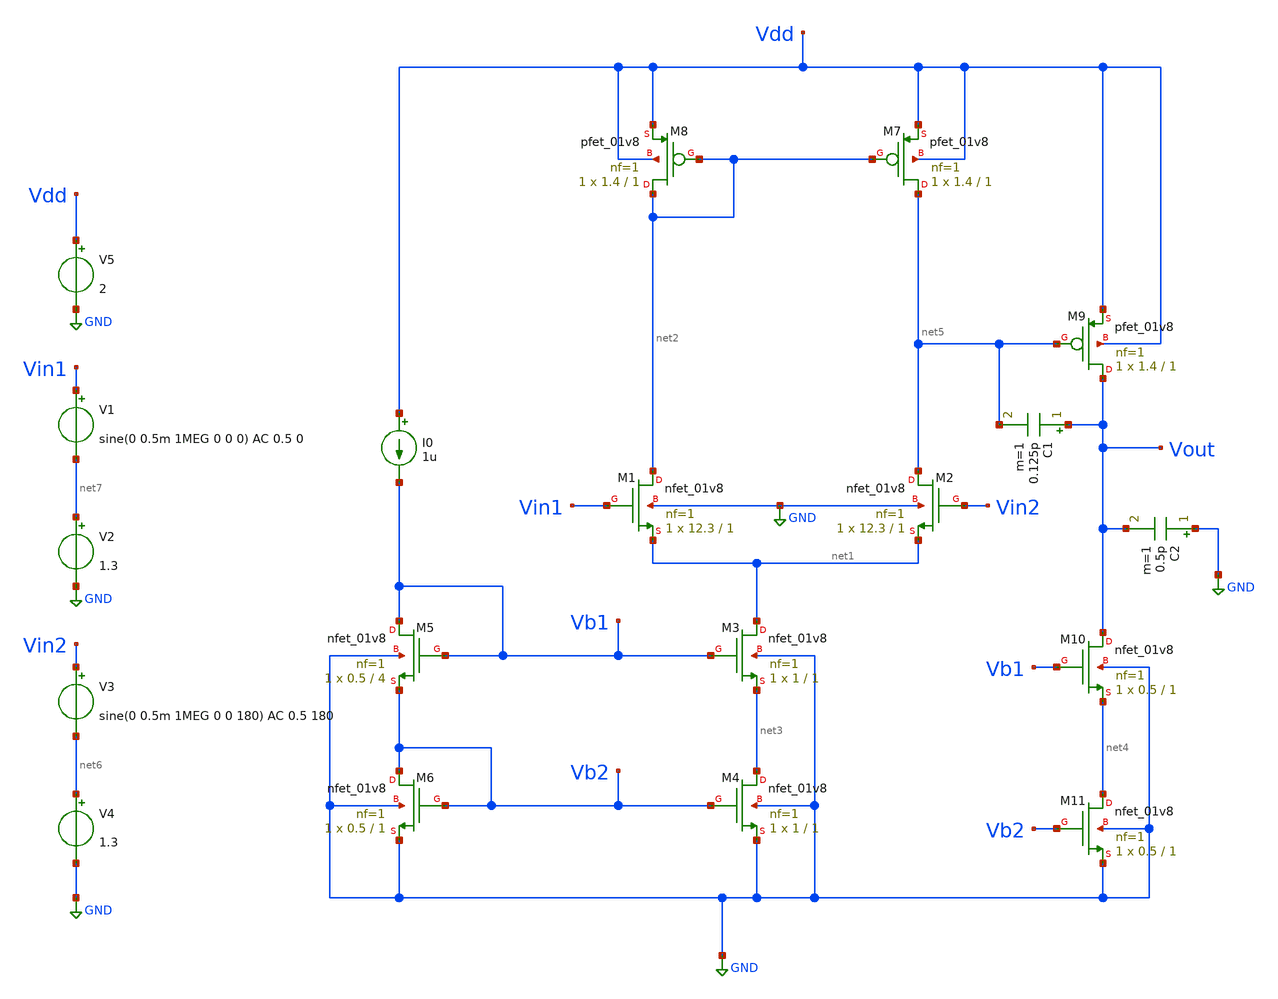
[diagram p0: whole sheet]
** sch_path: dacc.sch
**.subckt dacc
XM1 net2 Vin1 net1 GND sky130_fd_pr__nfet_01v8 L=1 W=12.3 nf=1 ad='int((nf+1)/2) * W/nf * 0.29' as='int((nf+2)/2) * W/nf * 0.29'
+ pd='2*int((nf+1)/2) * (W/nf + 0.29)' ps='2*int((nf+2)/2) * (W/nf + 0.29)' nrd='0.29 / W' nrs='0.29 / W'
+ sa=0 sb=0 sd=0 mult=1 m=1
XM2 net5 Vin2 net1 GND sky130_fd_pr__nfet_01v8 L=1 W=12.3 nf=1 ad='int((nf+1)/2) * W/nf * 0.29' as='int((nf+2)/2) * W/nf * 0.29'
+ pd='2*int((nf+1)/2) * (W/nf + 0.29)' ps='2*int((nf+2)/2) * (W/nf + 0.29)' nrd='0.29 / W' nrs='0.29 / W'
+ sa=0 sb=0 sd=0 mult=1 m=1
XM3 net1 Vb1 net3 GND sky130_fd_pr__nfet_01v8 L=1 W=1 nf=1 ad='int((nf+1)/2) * W/nf * 0.29' as='int((nf+2)/2) * W/nf * 0.29'
+ pd='2*int((nf+1)/2) * (W/nf + 0.29)' ps='2*int((nf+2)/2) * (W/nf + 0.29)' nrd='0.29 / W' nrs='0.29 / W'
+ sa=0 sb=0 sd=0 mult=1 m=1
XM4 net3 Vb2 GND GND sky130_fd_pr__nfet_01v8 L=1 W=1 nf=1 ad='int((nf+1)/2) * W/nf * 0.29' as='int((nf+2)/2) * W/nf * 0.29'
+ pd='2*int((nf+1)/2) * (W/nf + 0.29)' ps='2*int((nf+2)/2) * (W/nf + 0.29)' nrd='0.29 / W' nrs='0.29 / W'
+ sa=0 sb=0 sd=0 mult=1 m=1
XM5 Vb1 Vb1 Vb2 GND sky130_fd_pr__nfet_01v8 L=4 W=0.5 nf=1 ad='int((nf+1)/2) * W/nf * 0.29' as='int((nf+2)/2) * W/nf * 0.29'
+ pd='2*int((nf+1)/2) * (W/nf + 0.29)' ps='2*int((nf+2)/2) * (W/nf + 0.29)' nrd='0.29 / W' nrs='0.29 / W'
+ sa=0 sb=0 sd=0 mult=1 m=1
XM6 Vb2 Vb2 GND GND sky130_fd_pr__nfet_01v8 L=1 W=0.5 nf=1 ad='int((nf+1)/2) * W/nf * 0.29' as='int((nf+2)/2) * W/nf * 0.29'
+ pd='2*int((nf+1)/2) * (W/nf + 0.29)' ps='2*int((nf+2)/2) * (W/nf + 0.29)' nrd='0.29 / W' nrs='0.29 / W'
+ sa=0 sb=0 sd=0 mult=1 m=1
XM7 net5 net2 Vdd Vdd sky130_fd_pr__pfet_01v8 L=1 W=1.4 nf=1 ad='int((nf+1)/2) * W/nf * 0.29' as='int((nf+2)/2) * W/nf * 0.29'
+ pd='2*int((nf+1)/2) * (W/nf + 0.29)' ps='2*int((nf+2)/2) * (W/nf + 0.29)' nrd='0.29 / W' nrs='0.29 / W'
+ sa=0 sb=0 sd=0 mult=1 m=1
XM8 net2 net2 Vdd Vdd sky130_fd_pr__pfet_01v8 L=1 W=1.4 nf=1 ad='int((nf+1)/2) * W/nf * 0.29' as='int((nf+2)/2) * W/nf * 0.29'
+ pd='2*int((nf+1)/2) * (W/nf + 0.29)' ps='2*int((nf+2)/2) * (W/nf + 0.29)' nrd='0.29 / W' nrs='0.29 / W'
+ sa=0 sb=0 sd=0 mult=1 m=1
I0 Vdd Vb1 1u
XM9 Vout net5 Vdd Vdd sky130_fd_pr__pfet_01v8 L=1 W=1.4 nf=1 ad='int((nf+1)/2) * W/nf * 0.29' as='int((nf+2)/2) * W/nf * 0.29'
+ pd='2*int((nf+1)/2) * (W/nf + 0.29)' ps='2*int((nf+2)/2) * (W/nf + 0.29)' nrd='0.29 / W' nrs='0.29 / W'
+ sa=0 sb=0 sd=0 mult=1 m=1
XM10 Vout Vb1 net4 GND sky130_fd_pr__nfet_01v8 L=1 W=0.5 nf=1 ad='int((nf+1)/2) * W/nf * 0.29' as='int((nf+2)/2) * W/nf * 0.29'
+ pd='2*int((nf+1)/2) * (W/nf + 0.29)' ps='2*int((nf+2)/2) * (W/nf + 0.29)' nrd='0.29 / W' nrs='0.29 / W'
+ sa=0 sb=0 sd=0 mult=1 m=1
XM11 net4 Vb2 GND GND sky130_fd_pr__nfet_01v8 L=1 W=0.5 nf=1 ad='int((nf+1)/2) * W/nf * 0.29' as='int((nf+2)/2) * W/nf * 0.29'
+ pd='2*int((nf+1)/2) * (W/nf + 0.29)' ps='2*int((nf+2)/2) * (W/nf + 0.29)' nrd='0.29 / W' nrs='0.29 / W'
+ sa=0 sb=0 sd=0 mult=1 m=1
C1 Vout net5 0.125p m=1
C2 GND Vout 0.5p m=1
V1 Vin1 net7 sine(0 0.5m 1MEG 0 0 0) AC 0.5 0
V2 net7 GND 1.3
V3 Vin2 net6 sine(0 0.5m 1MEG 0 0 180) AC 0.5 180
V4 net6 GND 1.3
V5 Vdd GND 2
**** begin user architecture code

.lib /home/mallineni/eda_tools/open_pdks/sources/sky130_fd_pr/models/sky130.lib.spice tt

.control
set color0=white
set color1=black

* 1. TRANSIENT SIMULATION
tran 10n 5u
plot v(vin1) v(vout) title Transient_Vin_vs_Vout

* 2. AC FREQUENCY SWEEP
ac dec 20 1 100G

let g_db = db(v(vout))
let p_deg = (180/PI)*cph(v(vout))

meas ac dc_gain find g_db at=1
meas ac gbw when g_db=0
meas ac p_gbw find p_deg when g_db=0

print dc_gain gbw p_gbw

plot g_db title Bode_Gain_dB
plot p_deg title Bode_Phase_deg
.endc

**** end user architecture code
**.ends
.GLOBAL GND
.end
